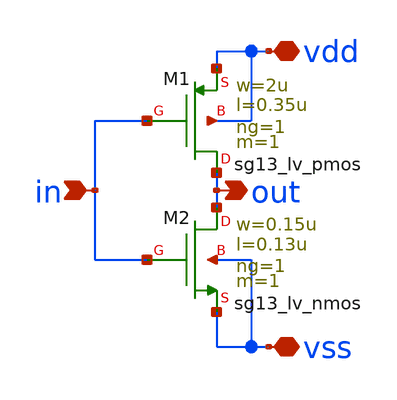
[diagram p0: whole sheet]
** sch_path: macros/heichips26_chronosense/schematic/xschem/inv.sch
* Copyright 2023 IHP PDK Authors
* Licensed under the Apache License, Version 2.0 (the "License");
* you may not use this file except in compliance with the License.
* You may obtain a copy of the License at
* https://www.apache.org/licenses/LICENSE-2.0
* Unless required by applicable law or agreed to in writing, software
* distributed under the License is distributed on an "AS IS" BASIS,
* WITHOUT WARRANTIES OR CONDITIONS OF ANY KIND, either express or implied.
* See the License for the specific language governing permissions and
* limitations under the License.
**.subckt inv in out vdd vss
*.ipin in
*.opin out
*.iopin vdd
*.iopin vss
XM1 out in vdd vdd sg13_lv_pmos w=2u l=0.35u ng=1 m=1 mm_ok=1
XM2 out in vss vss sg13_lv_nmos w=0.15u l=0.13u ng=1 m=1 mm_ok=1
**.ends
.end
